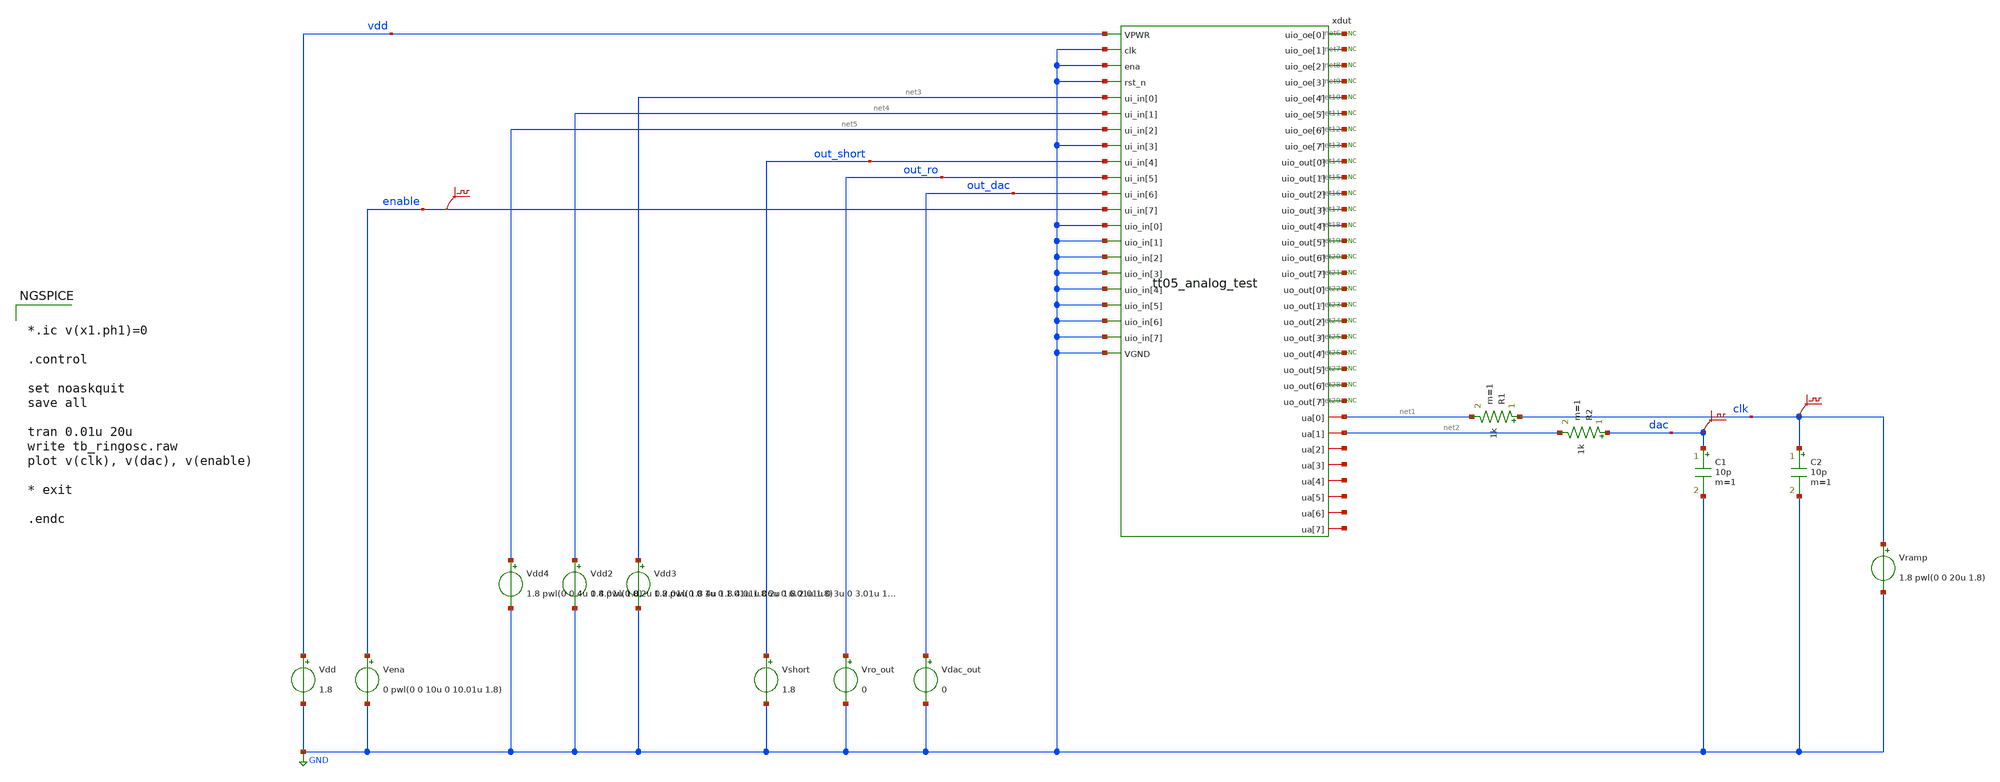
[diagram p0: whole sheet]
** sch_path: xschem/tb_tt05_analog_test_byp.sch
**.subckt tb_tt05_analog_test_byp
Vdd vdd GND 1.8
C1 dac GND 10p m=1
C2 clk GND 10p m=1
.save v(clk)
.save v(dac)
R1 clk net1 1k m=1
R2 dac net2 1k m=1
Vena enable GND 0 pwl(0 0 10u 0 10.01u 1.8)
xdut net6 net7 net8 net9 net10 net11 net12 net13 vdd net14 net15 GND net16 GND GND net17 net18 net19
+ net20 net3 net4 net21 net5 net22 GND net23 out_short out_ro net24 out_dac net25 enable net26 net27 GND
+ net28 GND net29 GND GND net1 GND net2 GND net30 GND net31 GND net32 net33 net34 net35 GND
+ tt05_analog_test
* noconn #net6
* noconn #net7
* noconn #net8
* noconn #net9
* noconn #net10
* noconn #net11
* noconn #net12
* noconn #net13
* noconn #net15
* noconn #net16
* noconn #net17
* noconn #net18
* noconn #net19
* noconn #net20
* noconn #net21
* noconn #net14
* noconn #net23
* noconn #net24
* noconn #net25
* noconn #net26
* noconn #net27
* noconn #net28
* noconn #net29
* noconn #net22
Vdd3 net3 GND 1.8 pwl(0 0 1u 0 1.01u 1.8 2u 1.8 2.01u 0 3u 0 3.01u 1.8 4u 1.8 4.01u 0 5u 0 5.01u 1.8
+ 6u 1.8 6.01u 0 7u 0 7.01u 1.8)
Vdd2 net4 GND 1.8 pwl(0 0 2u 0 2.01u 1.8 4u 1.8 4.01u 06u 0 6.01u 1.8)
Vdd4 net5 GND 1.8 pwl(0 0 4u 0 4.01u 1.8)
.save v(enable)
Vshort out_short GND 1.8
Vro_out out_ro GND 0
Vdac_out out_dac GND 0
Vramp clk GND 1.8 pwl(0 0 20u 1.8)
**** begin user architecture code
 ** manual skywater pdks install (with patches applied)
* .lib $::SKYWATER_MODELS/models/sky130.lib.spice tt

** opencircuitdesign pdks install
.lib $::SKYWATER_MODELS/sky130.lib.spice.tt.red tt

.param mc_mm_switch=0
.param mc_pr_switch=0



*.ic v(x1.ph1)=0

.control

set noaskquit
save all

tran 0.01u 20u
write tb_ringosc.raw
plot v(clk), v(dac), v(enable)

* exit

.endc


**** end user architecture code
**.ends
.GLOBAL GND
.end
